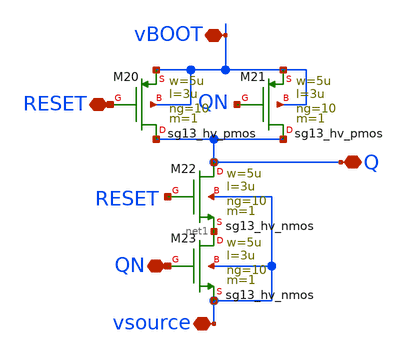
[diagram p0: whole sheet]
** sch_path: xschem/Floating_Gate/NAND1.sch
**.subckt NAND1 QN RESET vBOOT vsource Q
*.iopin QN
*.iopin RESET
*.iopin vBOOT
*.iopin vsource
*.iopin Q
XM20 Q RESET vBOOT vBOOT sg13_hv_pmos w=5u l=3u ng=10 m=1 mm_ok=1
XM21 Q QN vBOOT vBOOT sg13_hv_pmos w=5u l=3u ng=10 m=1 mm_ok=1
XM22 Q RESET net1 vsource sg13_hv_nmos w=5u l=3u ng=10 m=1 mm_ok=1
XM23 net1 QN vsource vsource sg13_hv_nmos w=5u l=3u ng=10 m=1 mm_ok=1
**.ends
.end
